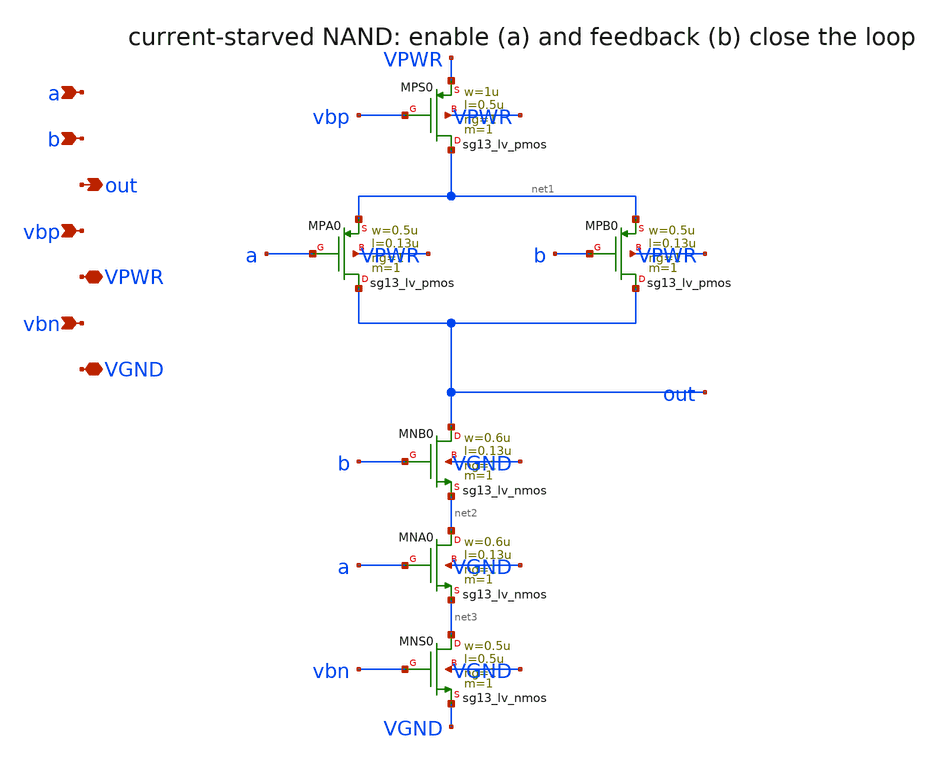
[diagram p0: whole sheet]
** sch_path: analog/xschem/csro_nand.sch
**.subckt csro_nand a b out vbp VPWR vbn VGND
*.ipin a
*.ipin b
*.opin out
*.ipin vbp
*.iopin VPWR
*.ipin vbn
*.iopin VGND
XMPS0 net1 vbp VPWR VPWR sg13_lv_pmos w=1u l=0.5u ng=1 m=1 mm_ok=1
XMPA0 out a net1 VPWR sg13_lv_pmos w=0.5u l=0.13u ng=1 m=1 mm_ok=1
XMPB0 out b net1 VPWR sg13_lv_pmos w=0.5u l=0.13u ng=1 m=1 mm_ok=1
XMNB0 out b net2 VGND sg13_lv_nmos w=0.6u l=0.13u ng=1 m=1 mm_ok=1
XMNA0 net2 a net3 VGND sg13_lv_nmos w=0.6u l=0.13u ng=1 m=1 mm_ok=1
XMNS0 net3 vbn VGND VGND sg13_lv_nmos w=0.5u l=0.5u ng=1 m=1 mm_ok=1
**.ends
.end
